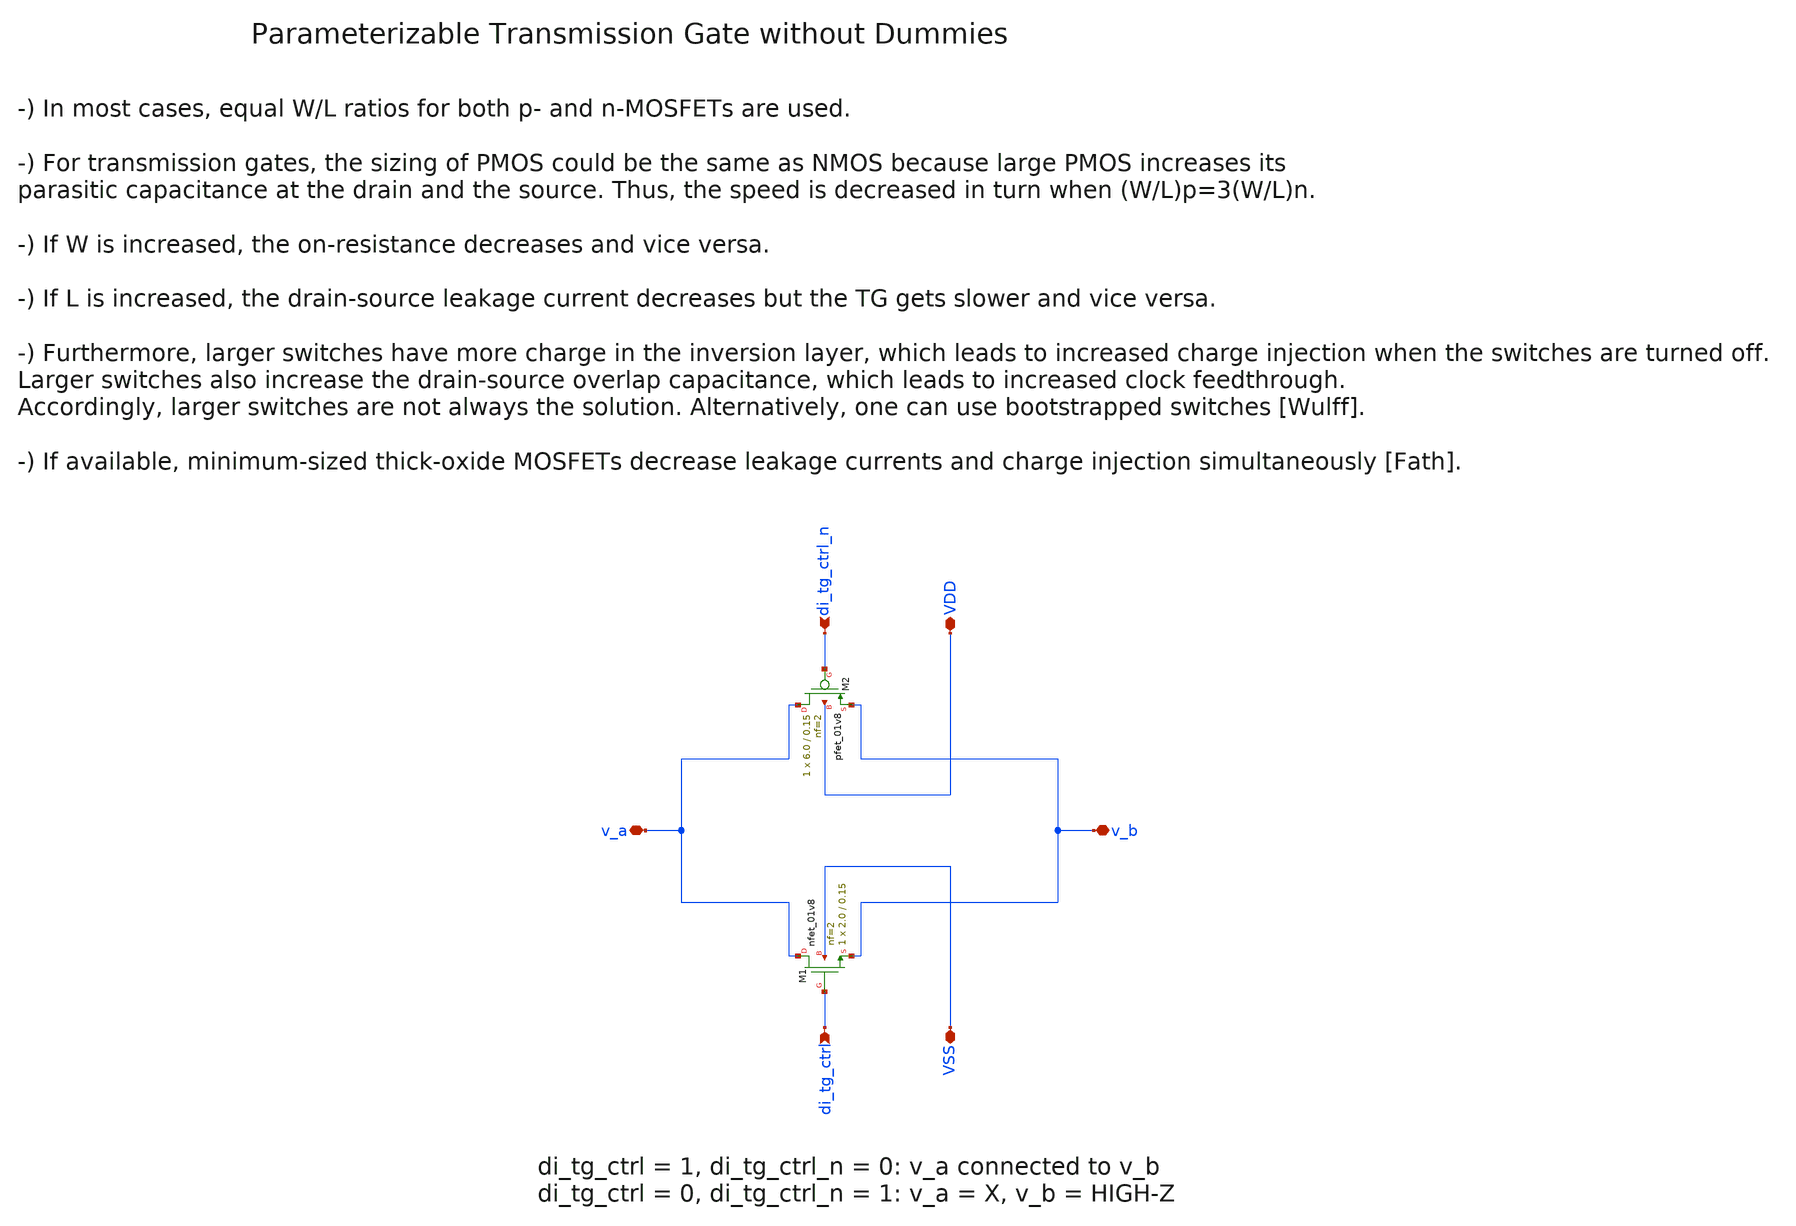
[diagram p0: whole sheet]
** sch_path: sky130/macros/iqmod/schematic/wspr_tx_iqmod_mixer_lo_logic_tg.sch
**.subckt wspr_tx_iqmod_mixer_lo_logic_tg v_a v_b VDD VSS di_tg_ctrl di_tg_ctrl_n
*.iopin v_a
*.iopin v_b
*.iopin VDD
*.iopin VSS
*.ipin di_tg_ctrl
*.ipin di_tg_ctrl_n
XM1 v_a di_tg_ctrl v_b VSS sky130_fd_pr__nfet_01v8 L=0.15 W=2.0 nf=2 ad='int((2 + 1)/2) * 2.0 / 2 * 0.29'
+ as='int((2 + 2)/2) * 2.0 / 2 * 0.29' pd='2*int((2 + 1)/2) * (2.0 / 2 + 0.29)' ps='2*int((2 + 2)/2) * (2.0 / 2 + 0.29)'
+ nrd='0.29 / 2.0 ' nrs='0.29 / 2.0 ' sa=0 sb=0 sd=0 mult=1 m=1
XM2 v_a di_tg_ctrl_n v_b VDD sky130_fd_pr__pfet_01v8 L=0.15 W=6.0 nf=2 ad='int((2 + 1)/2) * 6.0 / 2 * 0.29'
+ as='int((2 + 2)/2) * 6.0 / 2 * 0.29' pd='2*int((2 + 1)/2) * (6.0 / 2 + 0.29)' ps='2*int((2 + 2)/2) * (6.0 / 2 + 0.29)'
+ nrd='0.29 / 6.0 ' nrs='0.29 / 6.0 ' sa=0 sb=0 sd=0 mult=1 m=1
**.ends
.end
